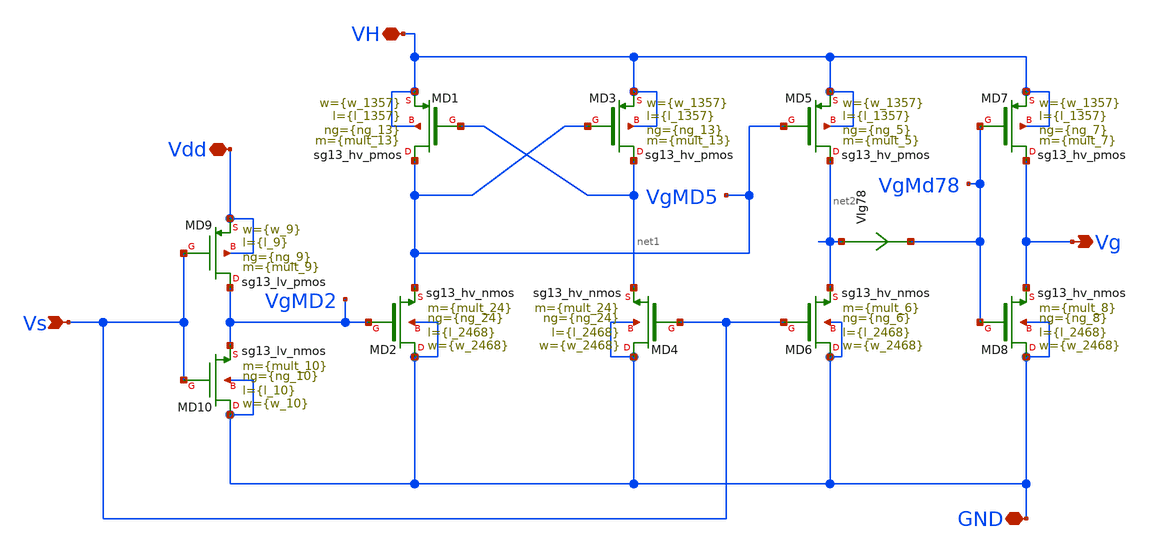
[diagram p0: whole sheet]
** sch_path: ChipUSM_AnalogTrack24/GD/GateDriver.sch
**.subckt GateDriver VH Vdd Vs Vg GND
*.iopin VH
*.iopin Vdd
*.ipin Vs
*.opin Vg
*.iopin GND
XMD9 VgMD2 Vs Vdd Vdd sg13_lv_pmos w={w_9} l={l_9} ng={ng_9} m={mult_9} mm_ok=1
XMD10 GND Vs VgMD2 GND sg13_lv_nmos w={w_10} l={l_10} ng={ng_10} m={mult_10} mm_ok=1
XMD1 VgMD5 net1 VH VH sg13_hv_pmos w={w_1357} l={l_1357} ng={ng_13} m={mult_13} mm_ok=1
XMD3 net1 VgMD5 VH VH sg13_hv_pmos w={w_1357} l={l_1357} ng={ng_13} m={mult_13} mm_ok=1
XMD5 net2 VgMD5 VH VH sg13_hv_pmos w={w_1357} l={l_1357} ng={ng_5} m={mult_5} mm_ok=1
XMD7 Vg VgMd78 VH VH sg13_hv_pmos w={w_1357} l={l_1357} ng={ng_7} m={mult_7} mm_ok=1
XMD2 GND VgMD2 VgMD5 GND sg13_hv_nmos w={w_2468} l={l_2468} ng={ng_24} m={mult_24} mm_ok=1
XMD4 GND Vs net1 GND sg13_hv_nmos w={w_2468} l={l_2468} ng={ng_24} m={mult_24} mm_ok=1
XMD6 GND Vs net2 GND sg13_hv_nmos w={w_2468} l={l_2468} ng={ng_6} m={mult_6} mm_ok=1
XMD8 GND VgMd78 Vg GND sg13_hv_nmos w={w_2468} l={l_2468} ng={ng_8} m={mult_8} mm_ok=1
VIg78 net2 VgMd78 0
.save i(vig78)
**.ends
.end
